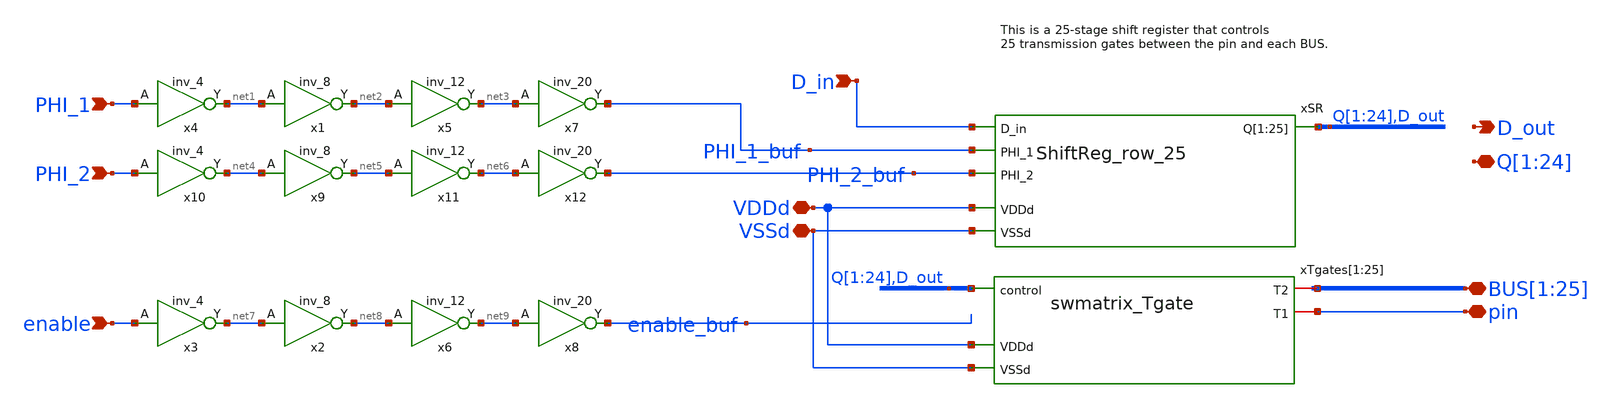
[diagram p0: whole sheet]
** sch_path: swmatrix_row_25/swmatrix_row_25_w_clkbuf.sch
**.subckt swmatrix_row_25_w_clkbuf pin PHI_2 PHI_1
*+ BUS[1],BUS[2],BUS[3],BUS[4],BUS[5],BUS[6],BUS[7],BUS[8],BUS[9],BUS[10],BUS[11],BUS[12],BUS[13],BUS[14],BUS[15],BUS[16],BUS[17],BUS[18],BUS[19],BUS[20],BUS[21],BUS[22],BUS[23],BUS[24],BUS[25] D_in
*+ Q[1],Q[2],Q[3],Q[4],Q[5],Q[6],Q[7],Q[8],Q[9],Q[10],Q[11],Q[12],Q[13],Q[14],Q[15],Q[16],Q[17],Q[18],Q[19],Q[20],Q[21],Q[22],Q[23],Q[24] VDDd VSSd D_out enable
*.iopin pin
*.ipin PHI_2
*.ipin PHI_1
*.iopin
*+ BUS[1],BUS[2],BUS[3],BUS[4],BUS[5],BUS[6],BUS[7],BUS[8],BUS[9],BUS[10],BUS[11],BUS[12],BUS[13],BUS[14],BUS[15],BUS[16],BUS[17],BUS[18],BUS[19],BUS[20],BUS[21],BUS[22],BUS[23],BUS[24],BUS[25]
*.ipin D_in
*.iopin
*+ Q[1],Q[2],Q[3],Q[4],Q[5],Q[6],Q[7],Q[8],Q[9],Q[10],Q[11],Q[12],Q[13],Q[14],Q[15],Q[16],Q[17],Q[18],Q[19],Q[20],Q[21],Q[22],Q[23],Q[24]
*.iopin VDDd
*.iopin VSSd
*.opin D_out
*.ipin enable
xSR Q[1] Q[2] Q[3] Q[4] Q[5] Q[6] Q[7] Q[8] Q[9] Q[10] Q[11] Q[12] Q[13] Q[14] Q[15] Q[16] Q[17]
+ Q[18] Q[19] Q[20] Q[21] Q[22] Q[23] Q[24] D_out D_in PHI_1_buf PHI_2_buf VDDd VSSd ShiftReg_row_25
xTgates[1] Q[1] BUS[1] pin VDDd VSSd swmatrix_Tgate
xTgates[2] Q[2] BUS[2] pin VDDd VSSd swmatrix_Tgate
xTgates[3] Q[3] BUS[3] pin VDDd VSSd swmatrix_Tgate
xTgates[4] Q[4] BUS[4] pin VDDd VSSd swmatrix_Tgate
xTgates[5] Q[5] BUS[5] pin VDDd VSSd swmatrix_Tgate
xTgates[6] Q[6] BUS[6] pin VDDd VSSd swmatrix_Tgate
xTgates[7] Q[7] BUS[7] pin VDDd VSSd swmatrix_Tgate
xTgates[8] Q[8] BUS[8] pin VDDd VSSd swmatrix_Tgate
xTgates[9] Q[9] BUS[9] pin VDDd VSSd swmatrix_Tgate
xTgates[10] Q[10] BUS[10] pin VDDd VSSd swmatrix_Tgate
xTgates[11] Q[11] BUS[11] pin VDDd VSSd swmatrix_Tgate
xTgates[12] Q[12] BUS[12] pin VDDd VSSd swmatrix_Tgate
xTgates[13] Q[13] BUS[13] pin VDDd VSSd swmatrix_Tgate
xTgates[14] Q[14] BUS[14] pin VDDd VSSd swmatrix_Tgate
xTgates[15] Q[15] BUS[15] pin VDDd VSSd swmatrix_Tgate
xTgates[16] Q[16] BUS[16] pin VDDd VSSd swmatrix_Tgate
xTgates[17] Q[17] BUS[17] pin VDDd VSSd swmatrix_Tgate
xTgates[18] Q[18] BUS[18] pin VDDd VSSd swmatrix_Tgate
xTgates[19] Q[19] BUS[19] pin VDDd VSSd swmatrix_Tgate
xTgates[20] Q[20] BUS[20] pin VDDd VSSd swmatrix_Tgate
xTgates[21] Q[21] BUS[21] pin VDDd VSSd swmatrix_Tgate
xTgates[22] Q[22] BUS[22] pin VDDd VSSd swmatrix_Tgate
xTgates[23] Q[23] BUS[23] pin VDDd VSSd swmatrix_Tgate
xTgates[24] Q[24] BUS[24] pin VDDd VSSd swmatrix_Tgate
xTgates[25] D_out BUS[25] pin VDDd VSSd swmatrix_Tgate
x1 net1 VSSd VDDd VSSd VDDd net2 gf180mcu_fd_sc_mcu9t5v0__inv_8
x4 PHI_1 VSSd VDDd VSSd VDDd net1 gf180mcu_fd_sc_mcu9t5v0__inv_4
x5 net2 VSSd VDDd VSSd VDDd net3 gf180mcu_fd_sc_mcu9t5v0__inv_12
x7 net3 PHI_1_buf VDDd VDDd VSSd VSSd gf180mcu_fd_sc_mcu9t5v0__inv_20
x9 net4 VSSd VDDd VSSd VDDd net5 gf180mcu_fd_sc_mcu9t5v0__inv_8
x10 PHI_2 VSSd VDDd VSSd VDDd net4 gf180mcu_fd_sc_mcu9t5v0__inv_4
x11 net5 VSSd VDDd VSSd VDDd net6 gf180mcu_fd_sc_mcu9t5v0__inv_12
x12 net6 PHI_2_buf VDDd VDDd VSSd VSSd gf180mcu_fd_sc_mcu9t5v0__inv_20
x2 net7 VSSd VDDd VSSd VDDd net8 gf180mcu_fd_sc_mcu9t5v0__inv_8
x3 enable VSSd VDDd VSSd VDDd net7 gf180mcu_fd_sc_mcu9t5v0__inv_4
x6 net8 VSSd VDDd VSSd VDDd net9 gf180mcu_fd_sc_mcu9t5v0__inv_12
x8 net9 enable_buf VDDd VDDd VSSd VSSd gf180mcu_fd_sc_mcu9t5v0__inv_20
**.ends
.end
